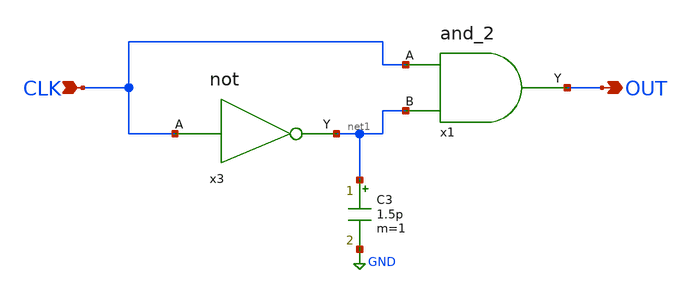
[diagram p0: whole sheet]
** sch_path: Circuiti/latches_sch_sym/edg_det.sch
**.subckt edg_det CLK OUT
*.ipin CLK
*.opin OUT
x3 CLK net1 not
C3 net1 GND 1.5p m=1
x1 CLK OUT net1 and_2
**.ends

* expanding   symbol:  /home/matteo/Documenti/tesi/Circuiti/logic_gates_sch_sym/not.sym # of pins=2
** sym_path: Circuiti/logic_gates_sch_sym/not.sym
** sch_path: Circuiti/logic_gates_sch_sym/not.sch
.subckt not A Y
*.ipin A
*.opin Y
XM1 Y A GND GND sky130_fd_pr__nfet_01v8 L=0.45 W=1 nf=1 ad='int((nf+1)/2) * W/nf * 0.29' as='int((nf+2)/2) * W/nf * 0.29'
+ pd='2*int((nf+1)/2) * (W/nf + 0.29)' ps='2*int((nf+2)/2) * (W/nf + 0.29)' nrd='0.29 / W' nrs='0.29 / W'
+ sa=0 sb=0 sd=0 mult=1 m=1
XM2 Y A Vdd VDD sky130_fd_pr__pfet_01v8 L=0.45 W=4.8 nf=1 ad='int((nf+1)/2) * W/nf * 0.29' as='int((nf+2)/2) * W/nf * 0.29'
+ pd='2*int((nf+1)/2) * (W/nf + 0.29)' ps='2*int((nf+2)/2) * (W/nf + 0.29)' nrd='0.29 / W' nrs='0.29 / W'
+ sa=0 sb=0 sd=0 mult=1 m=1
.ends


* expanding   symbol:  /home/matteo/Documenti/tesi/Circuiti/logic_gates_sch_sym/and_2.sym # of
*+ pins=3
** sym_path: Circuiti/logic_gates_sch_sym/and_2.sym
** sch_path: Circuiti/logic_gates_sch_sym/and_2.sch
.subckt and_2 A Y B
*.ipin B
*.ipin A
*.opin Y
x1 A net1 B nand_2
x2 net1 Y not
.ends


* expanding   symbol:  /home/matteo/Documenti/tesi/Circuiti/logic_gates_sch_sym/nand_2.sym # of
*+ pins=3
** sym_path: Circuiti/logic_gates_sch_sym/nand_2.sym
** sch_path: Circuiti/logic_gates_sch_sym/nand_2.sch
.subckt nand_2 A Y B
*.ipin A
*.ipin B
*.opin Y
XM1 Y A net1 GND sky130_fd_pr__nfet_01v8 L=0.15 W=1 nf=1 ad='int((nf+1)/2) * W/nf * 0.29' as='int((nf+2)/2) * W/nf * 0.29'
+ pd='2*int((nf+1)/2) * (W/nf + 0.29)' ps='2*int((nf+2)/2) * (W/nf + 0.29)' nrd='0.29 / W' nrs='0.29 / W'
+ sa=0 sb=0 sd=0 mult=1 m=1
XM3 Y B Vdd VDD sky130_fd_pr__pfet_01v8 L=0.45 W=4.8 nf=1 ad='int((nf+1)/2) * W/nf * 0.29' as='int((nf+2)/2) * W/nf * 0.29'
+ pd='2*int((nf+1)/2) * (W/nf + 0.29)' ps='2*int((nf+2)/2) * (W/nf + 0.29)' nrd='0.29 / W' nrs='0.29 / W'
+ sa=0 sb=0 sd=0 mult=1 m=1
XM4 Y A Vdd VDD sky130_fd_pr__pfet_01v8 L=0.45 W=4.8 nf=1 ad='int((nf+1)/2) * W/nf * 0.29' as='int((nf+2)/2) * W/nf * 0.29'
+ pd='2*int((nf+1)/2) * (W/nf + 0.29)' ps='2*int((nf+2)/2) * (W/nf + 0.29)' nrd='0.29 / W' nrs='0.29 / W'
+ sa=0 sb=0 sd=0 mult=1 m=1
XM2 net1 B GND GND sky130_fd_pr__nfet_01v8 L=0.15 W=1 nf=1 ad='int((nf+1)/2) * W/nf * 0.29' as='int((nf+2)/2) * W/nf * 0.29'
+ pd='2*int((nf+1)/2) * (W/nf + 0.29)' ps='2*int((nf+2)/2) * (W/nf + 0.29)' nrd='0.29 / W' nrs='0.29 / W'
+ sa=0 sb=0 sd=0 mult=1 m=1
.ends

.GLOBAL GND
.GLOBAL Vdd
.end
